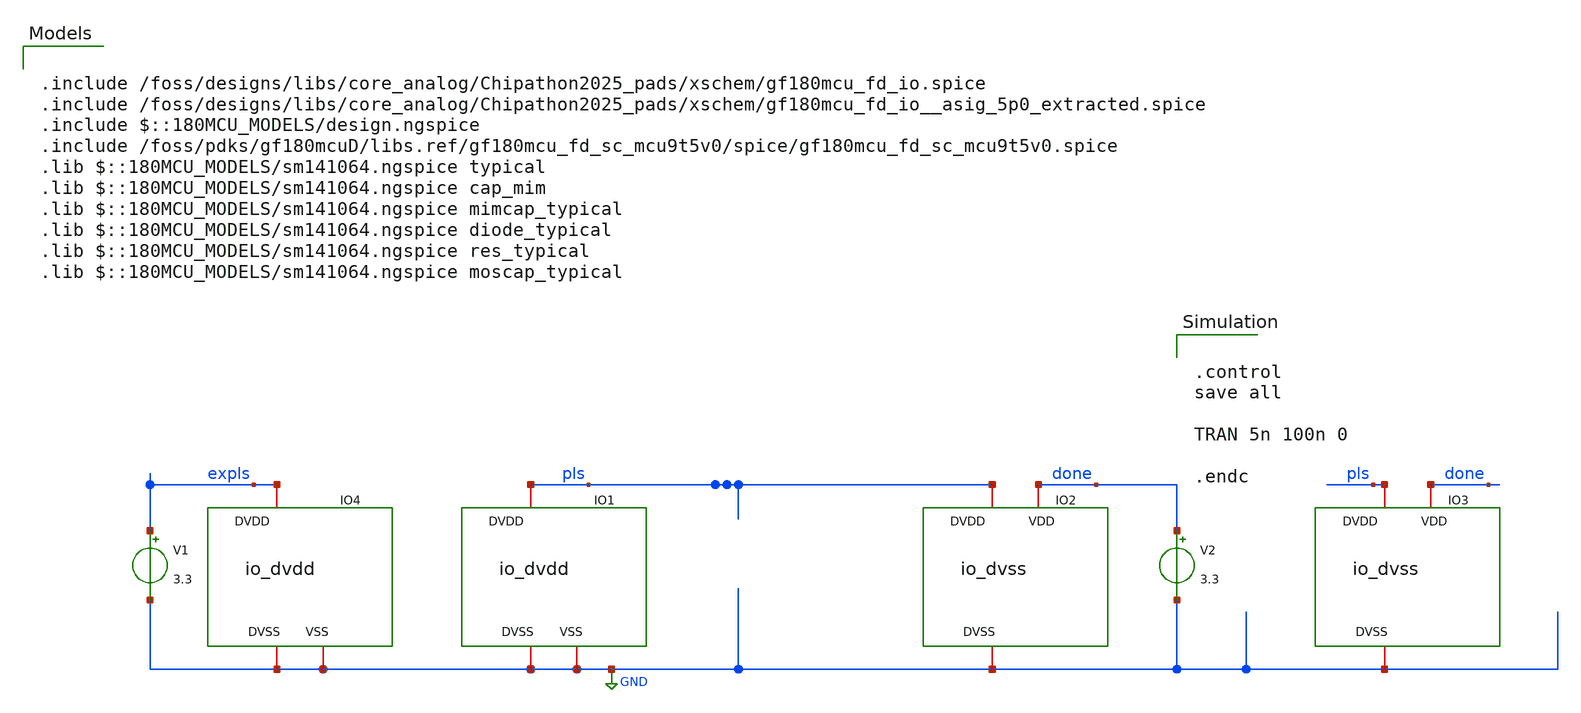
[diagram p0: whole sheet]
** sch_path: designs/dumexperiment.sch
**.subckt dumexperiment
XIO1 pls GND GND gf180mcu_fd_io__dvdd
V1 expls GND 3.3
XIO2 pls GND done gf180mcu_fd_io__dvss
V2 done GND 3.3
XIO3 pls GND done gf180mcu_fd_io__dvss
XIO4 expls GND GND gf180mcu_fd_io__dvdd
**** begin user architecture code

.include /foss/designs/libs/core_analog/Chipathon2025_pads/xschem/gf180mcu_fd_io.spice
.include /foss/designs/libs/core_analog/Chipathon2025_pads/xschem/gf180mcu_fd_io__asig_5p0_extracted.spice
.include $::180MCU_MODELS/design.ngspice
.include /foss/pdks/gf180mcuD/libs.ref/gf180mcu_fd_sc_mcu9t5v0/spice/gf180mcu_fd_sc_mcu9t5v0.spice
.lib $::180MCU_MODELS/sm141064.ngspice typical
.lib $::180MCU_MODELS/sm141064.ngspice cap_mim
.lib $::180MCU_MODELS/sm141064.ngspice mimcap_typical
.lib $::180MCU_MODELS/sm141064.ngspice diode_typical
.lib $::180MCU_MODELS/sm141064.ngspice res_typical
.lib $::180MCU_MODELS/sm141064.ngspice moscap_typical



.control
save all

TRAN 5n 100n 0

.endc


**** end user architecture code
**.ends
.GLOBAL GND
.end
